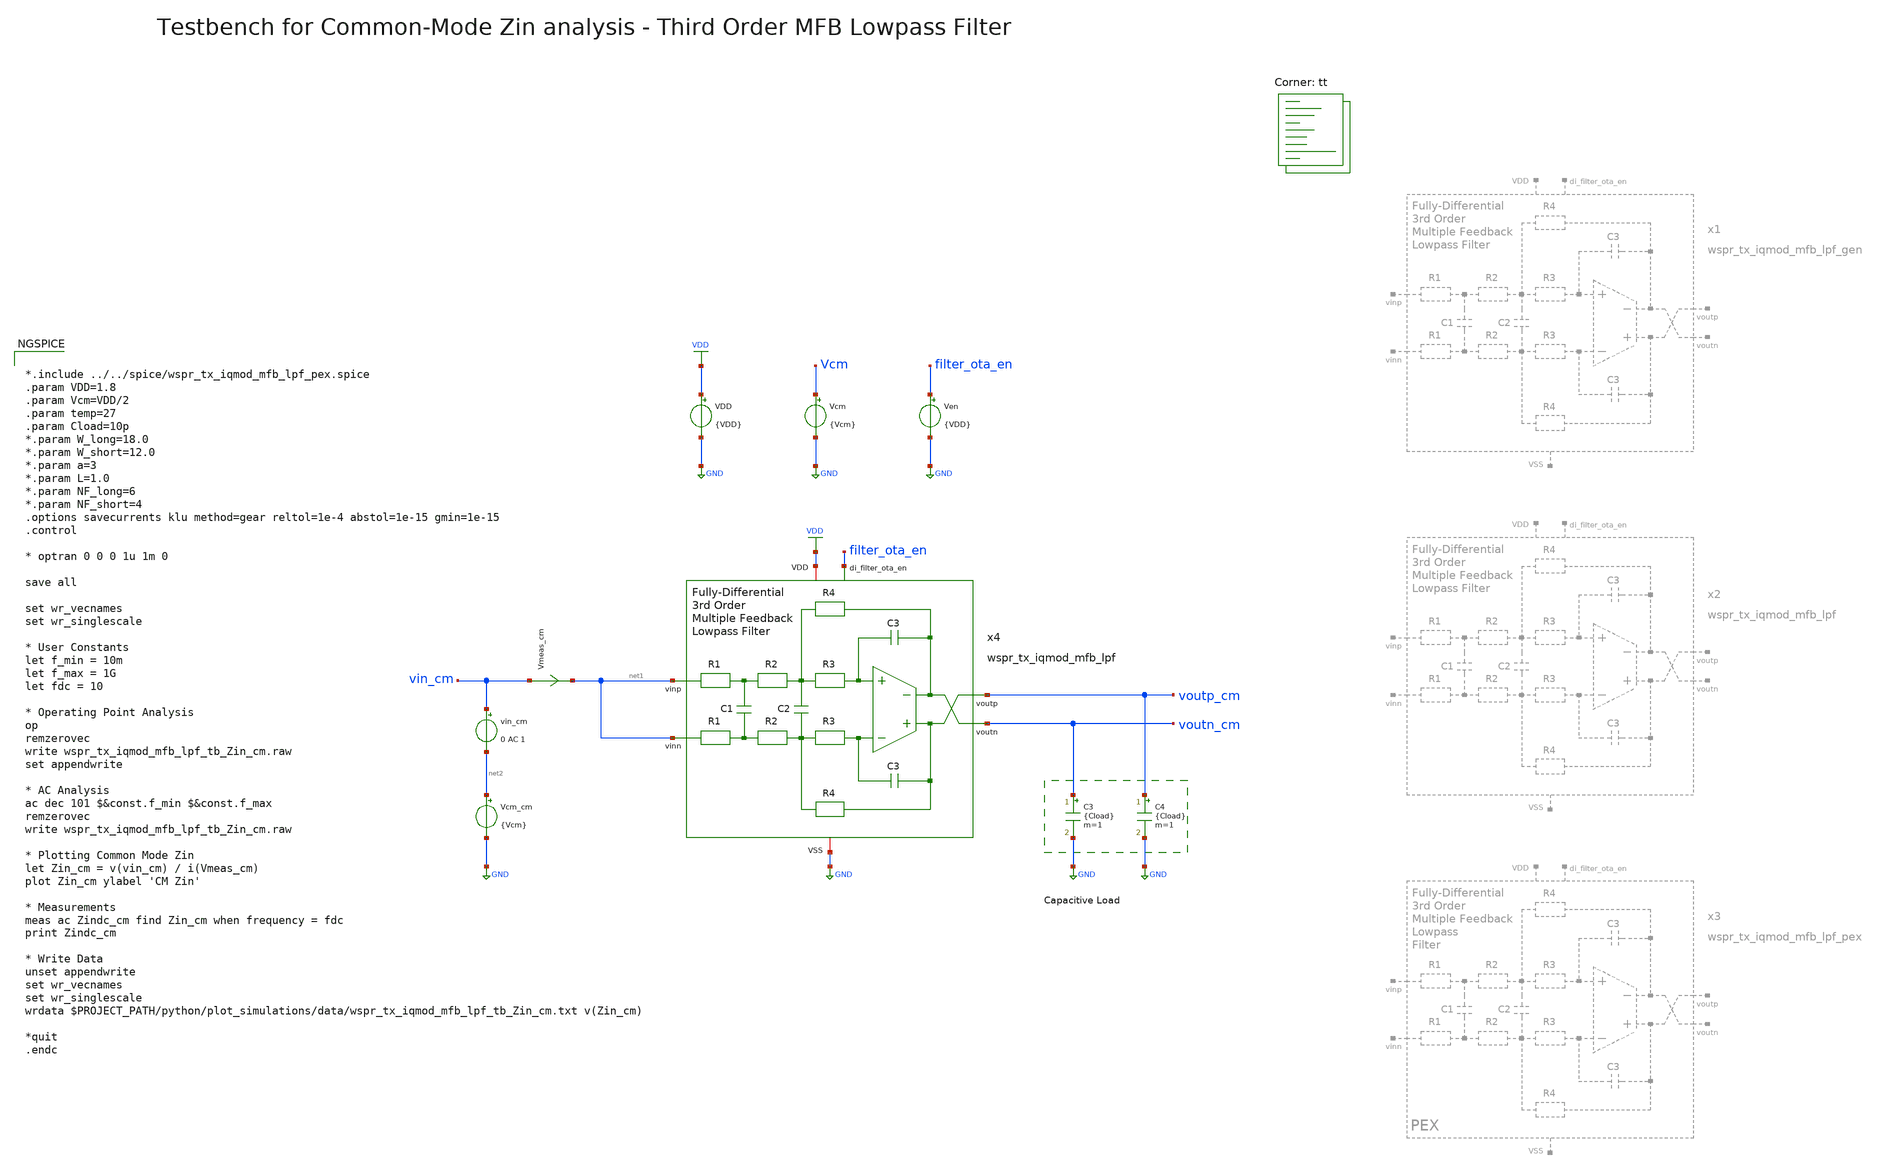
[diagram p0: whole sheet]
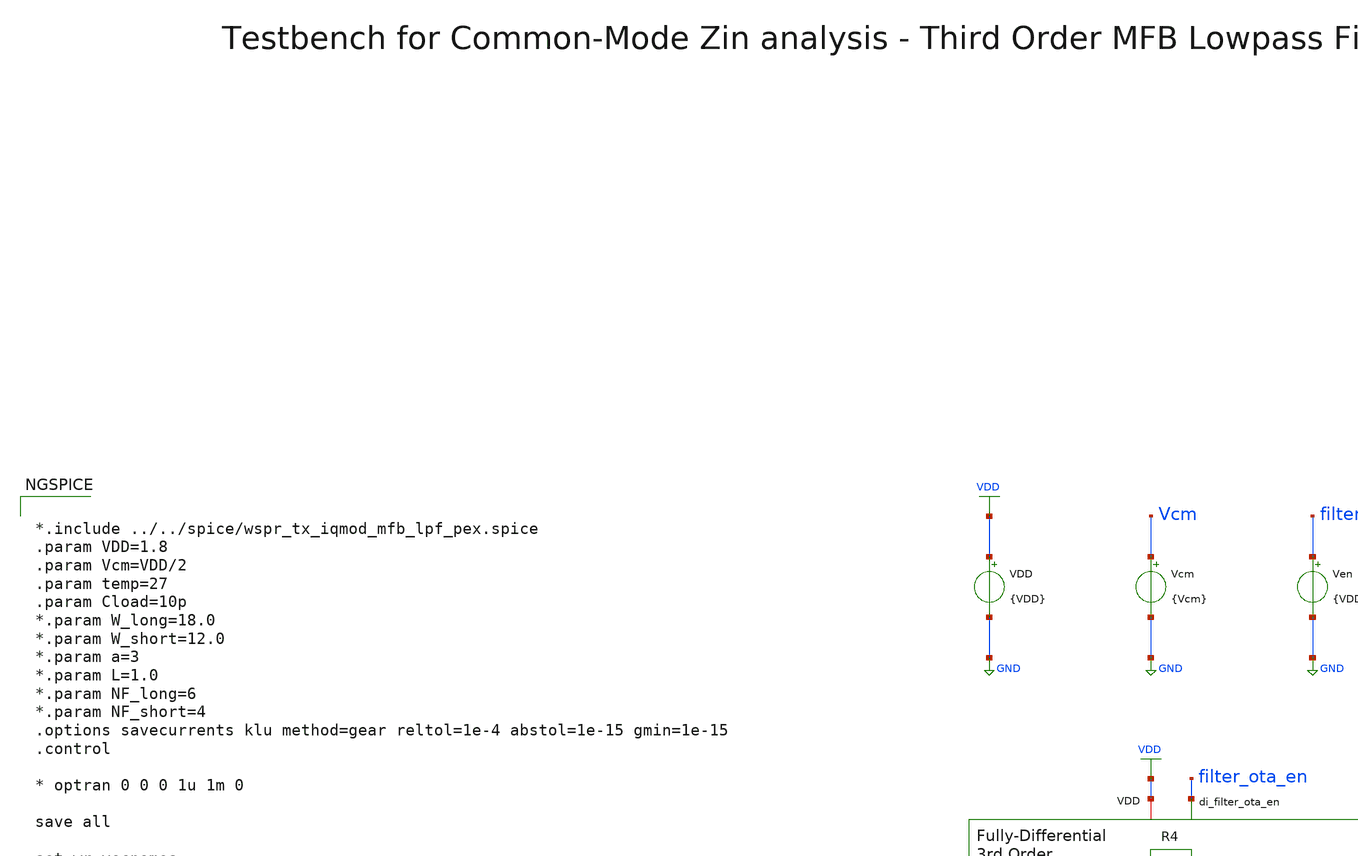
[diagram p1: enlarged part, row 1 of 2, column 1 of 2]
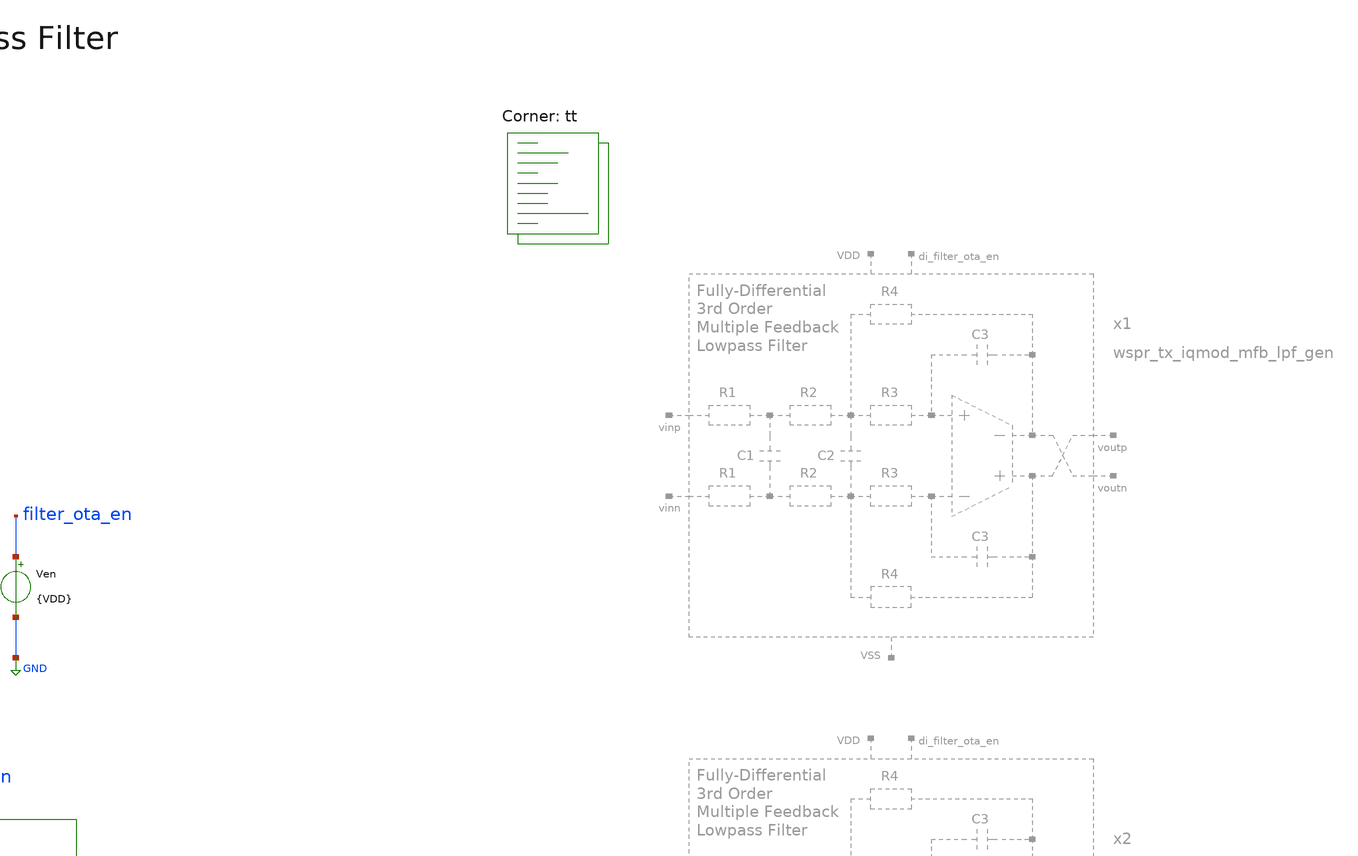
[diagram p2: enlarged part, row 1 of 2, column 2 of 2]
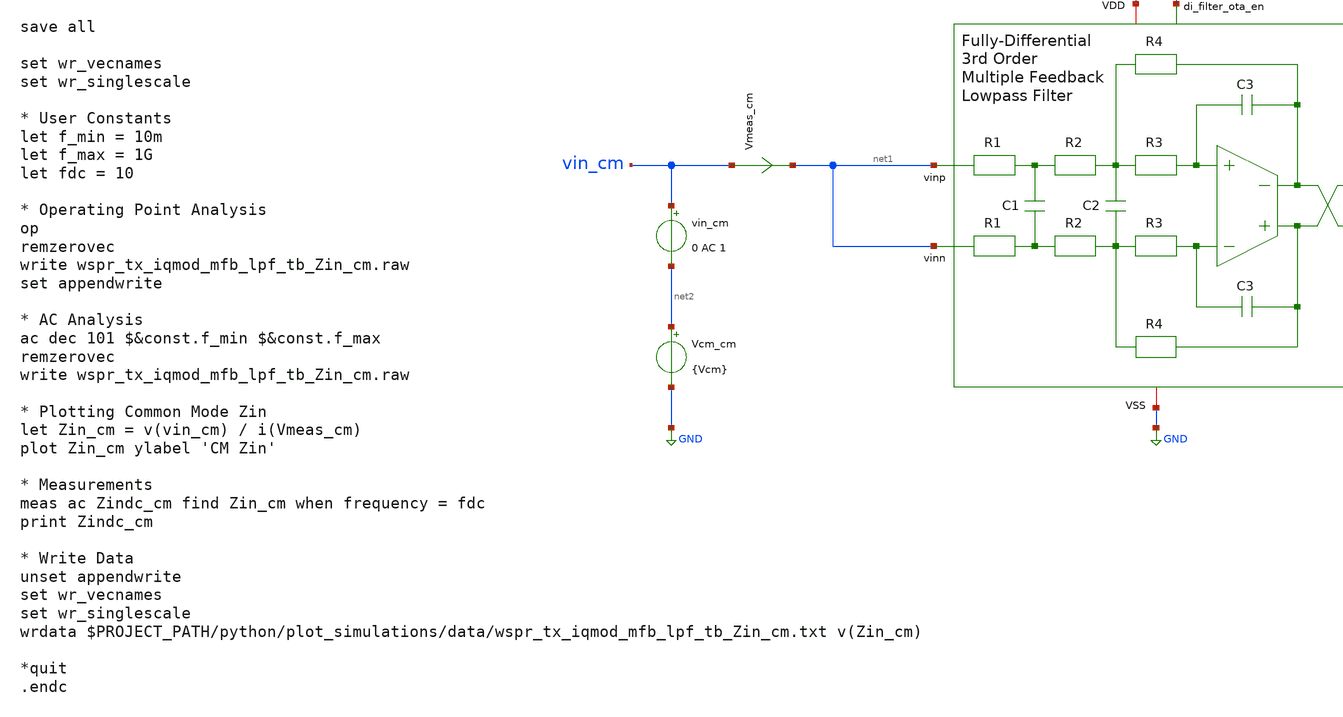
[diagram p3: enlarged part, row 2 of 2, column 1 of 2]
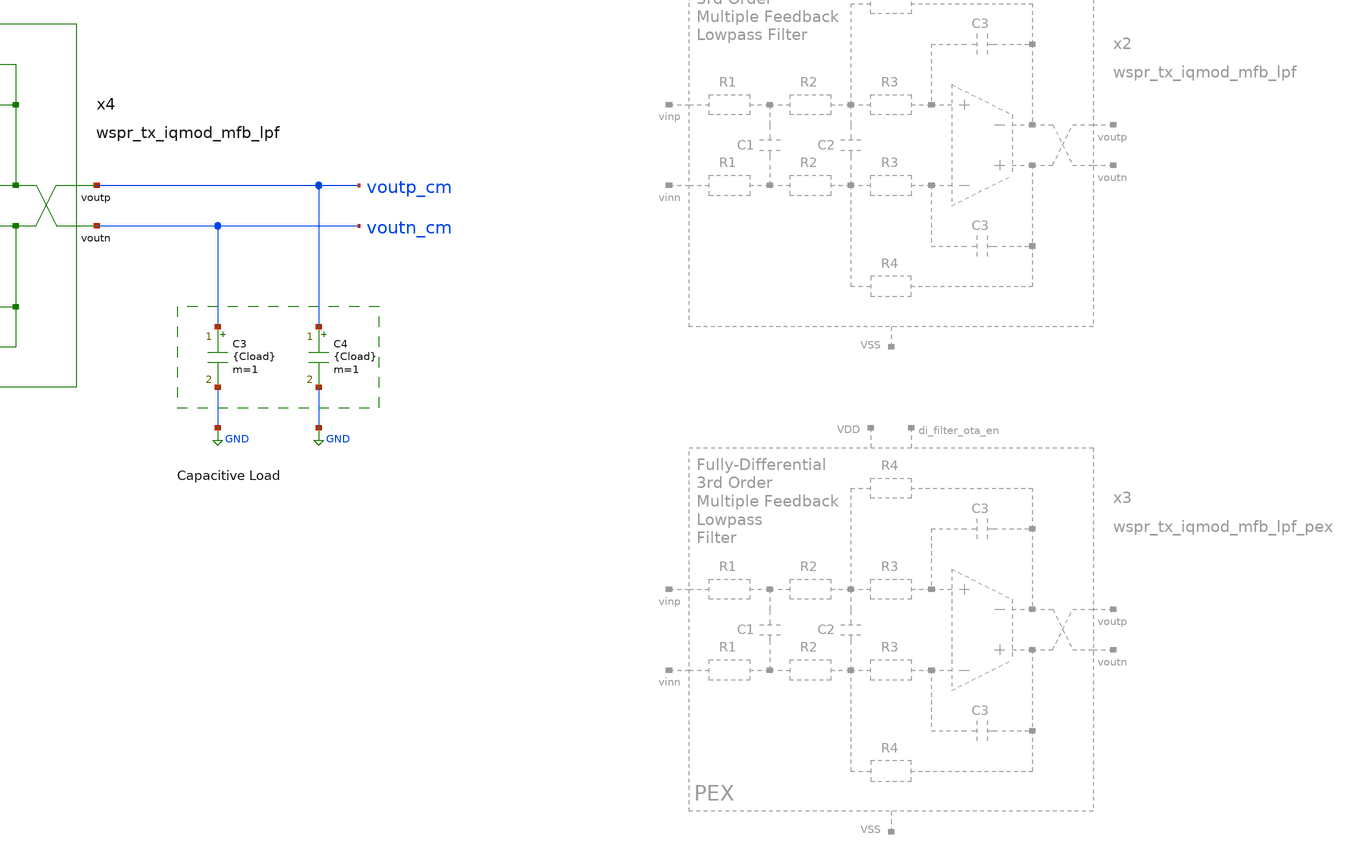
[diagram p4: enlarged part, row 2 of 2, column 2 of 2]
** sch_path: sky130/xschem/testbenches/wspr_tx_iqmod_mfb_lpf_tb_Zin_cm.sch
**.subckt wspr_tx_iqmod_mfb_lpf_tb_Zin_cm
C3 voutn_cm GND {Cload} m=1
C4 voutp_cm GND {Cload} m=1
vin_cm vin_cm net2 0 AC 1
Vmeas_cm vin_cm net1 0
.save i(vmeas_cm)
Vcm_cm net2 GND {Vcm}
VDD VDD GND {VDD}
Vcm Vcm GND {Vcm}
Ven filter_ota_en GND {VDD}
x4 filter_ota_en voutp_cm net1 voutn_cm net1 VDD GND wspr_tx_iqmod_mfb_lpf
**** begin user architecture code


*.include ../../spice/wspr_tx_iqmod_mfb_lpf_pex.spice
.param VDD=1.8
.param Vcm=VDD/2
.param temp=27
.param Cload=10p
*.param W_long=18.0
*.param W_short=12.0
*.param a=3
*.param L=1.0
*.param NF_long=6
*.param NF_short=4
.options savecurrents klu method=gear reltol=1e-4 abstol=1e-15 gmin=1e-15
.control

* optran 0 0 0 1u 1m 0

save all

set wr_vecnames
set wr_singlescale

* User Constants
let f_min = 10m
let f_max = 1G
let fdc = 10

* Operating Point Analysis
op
remzerovec
write wspr_tx_iqmod_mfb_lpf_tb_Zin_cm.raw
set appendwrite

* AC Analysis
ac dec 101 $&const.f_min $&const.f_max
remzerovec
write wspr_tx_iqmod_mfb_lpf_tb_Zin_cm.raw

* Plotting Common Mode Zin
let Zin_cm = v(vin_cm) / i(Vmeas_cm)
plot Zin_cm ylabel 'CM Zin'

* Measurements
meas ac Zindc_cm find Zin_cm when frequency = fdc
print Zindc_cm

* Write Data
unset appendwrite
set wr_vecnames
set wr_singlescale
wrdata $PROJECT_PATH/python/plot_simulations/data/wspr_tx_iqmod_mfb_lpf_tb_Zin_cm.txt v(Zin_cm)

*quit
.endc


.lib $::SKYWATER_MODELS/sky130.lib.spice tt
**** end user architecture code
**.ends
.GLOBAL GND
.GLOBAL VDD
.end
